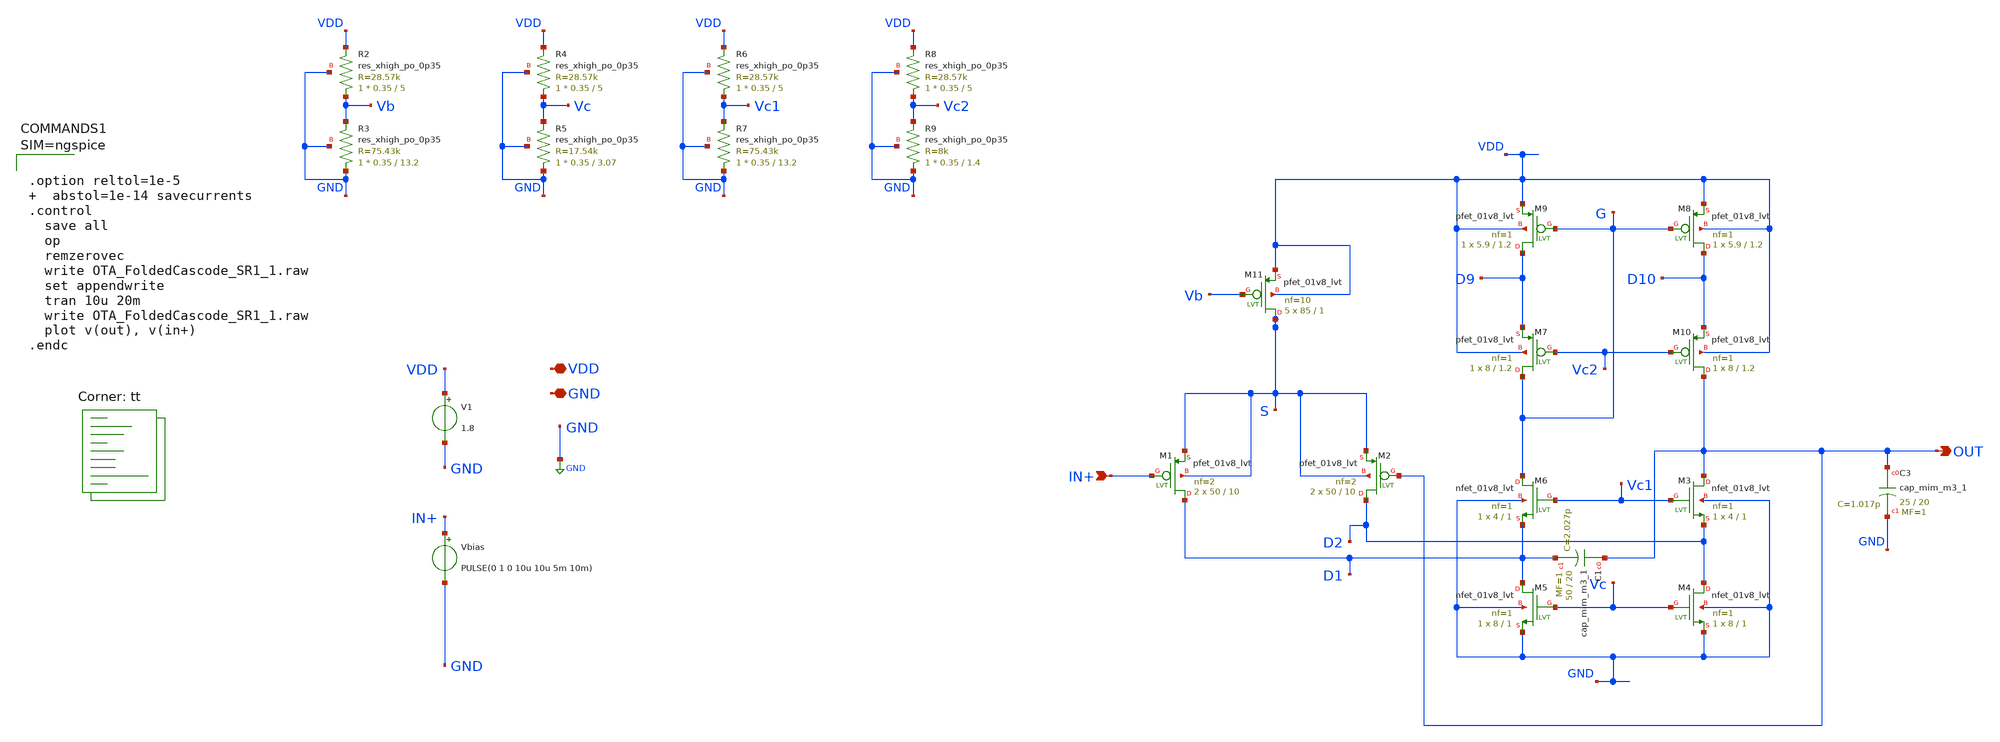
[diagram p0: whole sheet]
** sch_path: xschem/OTA_FoldedCascode_SR1_1.sch
**.subckt OTA_FoldedCascode_SR1_1 VDD GND OUT IN+
*.iopin VDD
*.iopin GND
*.opin OUT
*.ipin IN+
V1 VDD GND 1.8
Vbias IN+ GND PULSE(0 1 0 10u 10u 5m 10m)
XR2 Vb VDD GND sky130_fd_pr__res_xhigh_po_0p35 L=5 mult=1 m=1
XR3 GND Vb GND sky130_fd_pr__res_xhigh_po_0p35 L=13.2 mult=1 m=1
XR4 Vc VDD GND sky130_fd_pr__res_xhigh_po_0p35 L=5 mult=1 m=1
XR5 GND Vc GND sky130_fd_pr__res_xhigh_po_0p35 L=3.07 mult=1 m=1
XR6 Vc1 VDD GND sky130_fd_pr__res_xhigh_po_0p35 L=5 mult=1 m=1
XR7 GND Vc1 GND sky130_fd_pr__res_xhigh_po_0p35 L=13.2 mult=1 m=1
XR8 Vc2 VDD GND sky130_fd_pr__res_xhigh_po_0p35 L=5 mult=1 m=1
XR9 GND Vc2 GND sky130_fd_pr__res_xhigh_po_0p35 L=1.4 mult=1 m=1
XC3 OUT GND sky130_fd_pr__cap_mim_m3_1 W=25 L=20 MF=1 m=1
XM11 S Vb VDD VDD sky130_fd_pr__pfet_01v8_lvt L=1 W=85 nf=10 ad='int((nf+1)/2) * W/nf * 0.29' as='int((nf+2)/2) * W/nf * 0.29'
+ pd='2*int((nf+1)/2) * (W/nf + 0.29)' ps='2*int((nf+2)/2) * (W/nf + 0.29)' nrd='0.29 / W' nrs='0.29 / W'
+ sa=0 sb=0 sd=0 mult=5 m=5
XM1 D1 IN+ S S sky130_fd_pr__pfet_01v8_lvt L=10 W=50 nf=2 ad='int((nf+1)/2) * W/nf * 0.29' as='int((nf+2)/2) * W/nf * 0.29'
+ pd='2*int((nf+1)/2) * (W/nf + 0.29)' ps='2*int((nf+2)/2) * (W/nf + 0.29)' nrd='0.29 / W' nrs='0.29 / W'
+ sa=0 sb=0 sd=0 mult=2 m=2
XM2 D2 OUT S S sky130_fd_pr__pfet_01v8_lvt L=10 W=50 nf=2 ad='int((nf+1)/2) * W/nf * 0.29' as='int((nf+2)/2) * W/nf * 0.29'
+ pd='2*int((nf+1)/2) * (W/nf + 0.29)' ps='2*int((nf+2)/2) * (W/nf + 0.29)' nrd='0.29 / W' nrs='0.29 / W'
+ sa=0 sb=0 sd=0 mult=2 m=2
XM3 OUT Vc1 D2 GND sky130_fd_pr__nfet_01v8_lvt L=1 W=4 nf=1 ad='int((nf+1)/2) * W/nf * 0.29' as='int((nf+2)/2) * W/nf * 0.29'
+ pd='2*int((nf+1)/2) * (W/nf + 0.29)' ps='2*int((nf+2)/2) * (W/nf + 0.29)' nrd='0.29 / W' nrs='0.29 / W'
+ sa=0 sb=0 sd=0 mult=1 m=1
XM4 D2 Vc GND GND sky130_fd_pr__nfet_01v8_lvt L=1 W=8 nf=1 ad='int((nf+1)/2) * W/nf * 0.29' as='int((nf+2)/2) * W/nf * 0.29'
+ pd='2*int((nf+1)/2) * (W/nf + 0.29)' ps='2*int((nf+2)/2) * (W/nf + 0.29)' nrd='0.29 / W' nrs='0.29 / W'
+ sa=0 sb=0 sd=0 mult=1 m=1
XM5 D1 Vc GND GND sky130_fd_pr__nfet_01v8_lvt L=1 W=8 nf=1 ad='int((nf+1)/2) * W/nf * 0.29' as='int((nf+2)/2) * W/nf * 0.29'
+ pd='2*int((nf+1)/2) * (W/nf + 0.29)' ps='2*int((nf+2)/2) * (W/nf + 0.29)' nrd='0.29 / W' nrs='0.29 / W'
+ sa=0 sb=0 sd=0 mult=1 m=1
XM6 G Vc1 D1 GND sky130_fd_pr__nfet_01v8_lvt L=1 W=4 nf=1 ad='int((nf+1)/2) * W/nf * 0.29' as='int((nf+2)/2) * W/nf * 0.29'
+ pd='2*int((nf+1)/2) * (W/nf + 0.29)' ps='2*int((nf+2)/2) * (W/nf + 0.29)' nrd='0.29 / W' nrs='0.29 / W'
+ sa=0 sb=0 sd=0 mult=1 m=1
XM7 G Vc2 D9 VDD sky130_fd_pr__pfet_01v8_lvt L=1.2 W=8 nf=1 ad='int((nf+1)/2) * W/nf * 0.29' as='int((nf+2)/2) * W/nf * 0.29'
+ pd='2*int((nf+1)/2) * (W/nf + 0.29)' ps='2*int((nf+2)/2) * (W/nf + 0.29)' nrd='0.29 / W' nrs='0.29 / W'
+ sa=0 sb=0 sd=0 mult=1 m=1
XM9 D9 G VDD VDD sky130_fd_pr__pfet_01v8_lvt L=1.2 W=5.9 nf=1 ad='int((nf+1)/2) * W/nf * 0.29' as='int((nf+2)/2) * W/nf * 0.29'
+ pd='2*int((nf+1)/2) * (W/nf + 0.29)' ps='2*int((nf+2)/2) * (W/nf + 0.29)' nrd='0.29 / W' nrs='0.29 / W'
+ sa=0 sb=0 sd=0 mult=1 m=1
XM8 D10 G VDD VDD sky130_fd_pr__pfet_01v8_lvt L=1.2 W=5.9 nf=1 ad='int((nf+1)/2) * W/nf * 0.29' as='int((nf+2)/2) * W/nf * 0.29'
+ pd='2*int((nf+1)/2) * (W/nf + 0.29)' ps='2*int((nf+2)/2) * (W/nf + 0.29)' nrd='0.29 / W' nrs='0.29 / W'
+ sa=0 sb=0 sd=0 mult=1 m=1
XM10 OUT Vc2 D10 VDD sky130_fd_pr__pfet_01v8_lvt L=1.2 W=8 nf=1 ad='int((nf+1)/2) * W/nf * 0.29' as='int((nf+2)/2) * W/nf * 0.29'
+ pd='2*int((nf+1)/2) * (W/nf + 0.29)' ps='2*int((nf+2)/2) * (W/nf + 0.29)' nrd='0.29 / W' nrs='0.29 / W'
+ sa=0 sb=0 sd=0 mult=1 m=1
XC1 OUT D1 sky130_fd_pr__cap_mim_m3_1 W=50 L=20 MF=1 m=1
**** begin user architecture code



.option reltol=1e-5   abstol=1e-14 savecurrents
.control
  save all
  op
  remzerovec
  write OTA_FoldedCascode_SR1_1.raw
  set appendwrite
  tran 10u 20m
  write OTA_FoldedCascode_SR1_1.raw
  plot v(out), v(in+)
.endc



.lib $::SKYWATER_MODELS/sky130.lib.spice tt
**** end user architecture code
**.ends
.GLOBAL GND
.end
